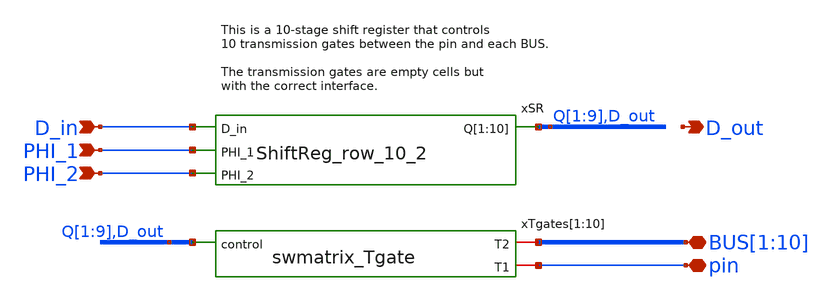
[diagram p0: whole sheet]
** sch_path: designs/switch_matrix_gf180mcu_9t5v0-main/designs/libs/core_swmatrix/swmatrix_row_10.sch
**.subckt swmatrix_row_10 pin PHI_2 PHI_1
*+ BUS[1],BUS[2],BUS[3],BUS[4],BUS[5],BUS[6],BUS[7],BUS[8],BUS[9],BUS[10] D_in D_out
*.iopin pin
*.ipin PHI_2
*.ipin PHI_1
*.iopin BUS[1],BUS[2],BUS[3],BUS[4],BUS[5],BUS[6],BUS[7],BUS[8],BUS[9],BUS[10]
*.ipin D_in
*.opin D_out
xSR Q[1] Q[2] Q[3] Q[4] Q[5] Q[6] Q[7] Q[8] Q[9] D_out D_in PHI_1 PHI_2 ShiftReg_row_10_2
xTgates[1] Q[1] BUS[1] pin swmatrix_Tgate
xTgates[2] Q[2] BUS[2] pin swmatrix_Tgate
xTgates[3] Q[3] BUS[3] pin swmatrix_Tgate
xTgates[4] Q[4] BUS[4] pin swmatrix_Tgate
xTgates[5] Q[5] BUS[5] pin swmatrix_Tgate
xTgates[6] Q[6] BUS[6] pin swmatrix_Tgate
xTgates[7] Q[7] BUS[7] pin swmatrix_Tgate
xTgates[8] Q[8] BUS[8] pin swmatrix_Tgate
xTgates[9] Q[9] BUS[9] pin swmatrix_Tgate
xTgates[10] D_out BUS[10] pin swmatrix_Tgate
**.ends
.end
